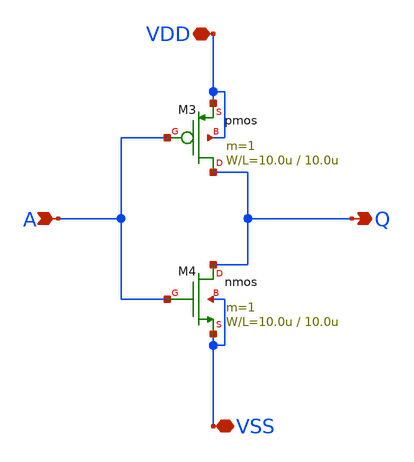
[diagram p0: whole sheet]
** sch_path: member_project/reodon/inverter_reodon_250719.sch
**.subckt inverter_reodon_250719 A Q VDD VSS
*.ipin A
*.opin Q
*.iopin VDD
*.iopin VSS
M3 Q A VDD VDD pmos L=10.0u W=10.0u m=1
M4 Q A VSS VSS nmos L=10.0u W=10.0u m=1
**.ends
.end
